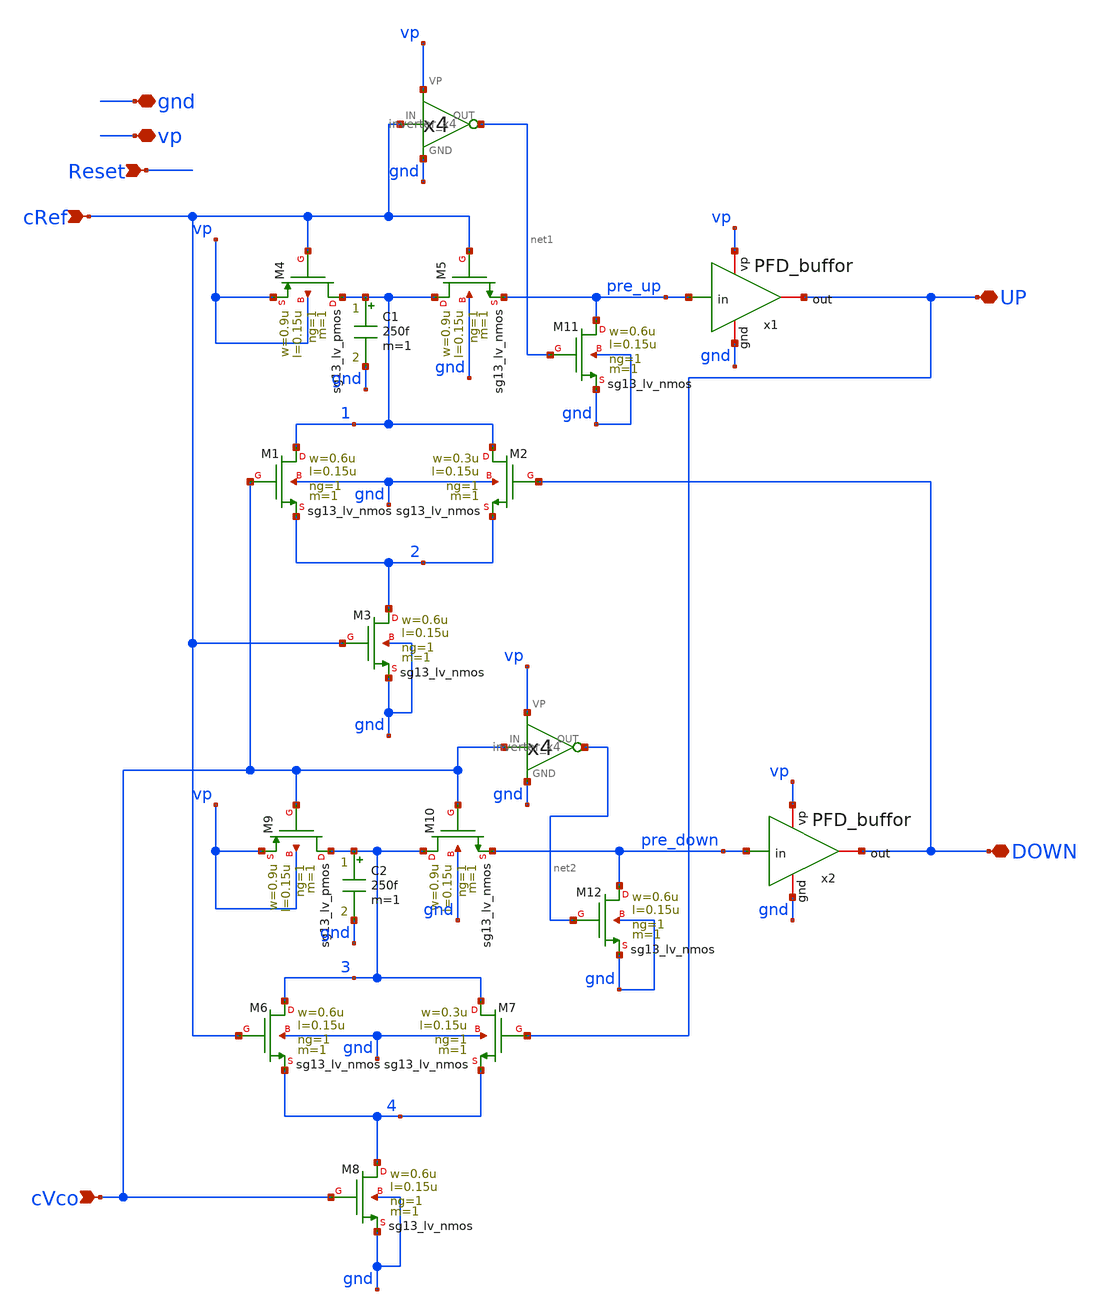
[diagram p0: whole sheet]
** sch_path: PFD/PFD_cell_withReset.sch
**.subckt PFD_cell_withReset gnd vp DOWN UP cRef cVco Reset
*.iopin gnd
*.iopin vp
*.iopin DOWN
*.iopin UP
*.ipin cRef
*.ipin cVco
*.ipin Reset
XM1 1 cVco 2 gnd sg13_lv_nmos w=0.6u l=0.15u ng=1 m=1 mm_ok=1
XM2 1 DOWN 2 gnd sg13_lv_nmos w=0.3u l=0.15u ng=1 m=1 mm_ok=1
XM3 2 cRef gnd gnd sg13_lv_nmos w=0.6u l=0.15u ng=1 m=1 mm_ok=1
XM6 3 cRef 4 gnd sg13_lv_nmos w=0.6u l=0.15u ng=1 m=1 mm_ok=1
XM7 3 UP 4 gnd sg13_lv_nmos w=0.3u l=0.15u ng=1 m=1 mm_ok=1
XM8 4 cVco gnd gnd sg13_lv_nmos w=0.6u l=0.15u ng=1 m=1 mm_ok=1
x1 gnd vp UP pre_up PFD_buffor
x2 gnd vp DOWN pre_down PFD_buffor
XM4 1 cRef vp vp sg13_lv_pmos w=0.9u l=0.15u ng=1 m=1 mm_ok=1
XM5 1 cRef pre_up gnd sg13_lv_nmos w=0.9u l=0.15u ng=1 m=1 mm_ok=1
XM9 3 cVco vp vp sg13_lv_pmos w=0.9u l=0.15u ng=1 m=1 mm_ok=1
XM10 3 cVco pre_down gnd sg13_lv_nmos w=0.9u l=0.15u ng=1 m=1 mm_ok=1
XM12 pre_down net2 gnd gnd sg13_lv_nmos w=0.6u l=0.15u ng=1 m=1 mm_ok=1
x3 cRef net1 vp gnd inverter_x4
x4 cVco net2 vp gnd inverter_x4
XM11 pre_up net1 gnd gnd sg13_lv_nmos w=0.6u l=0.15u ng=1 m=1 mm_ok=1
C2 3 gnd 250f m=1
C1 1 gnd 250f m=1
**.ends
.end
